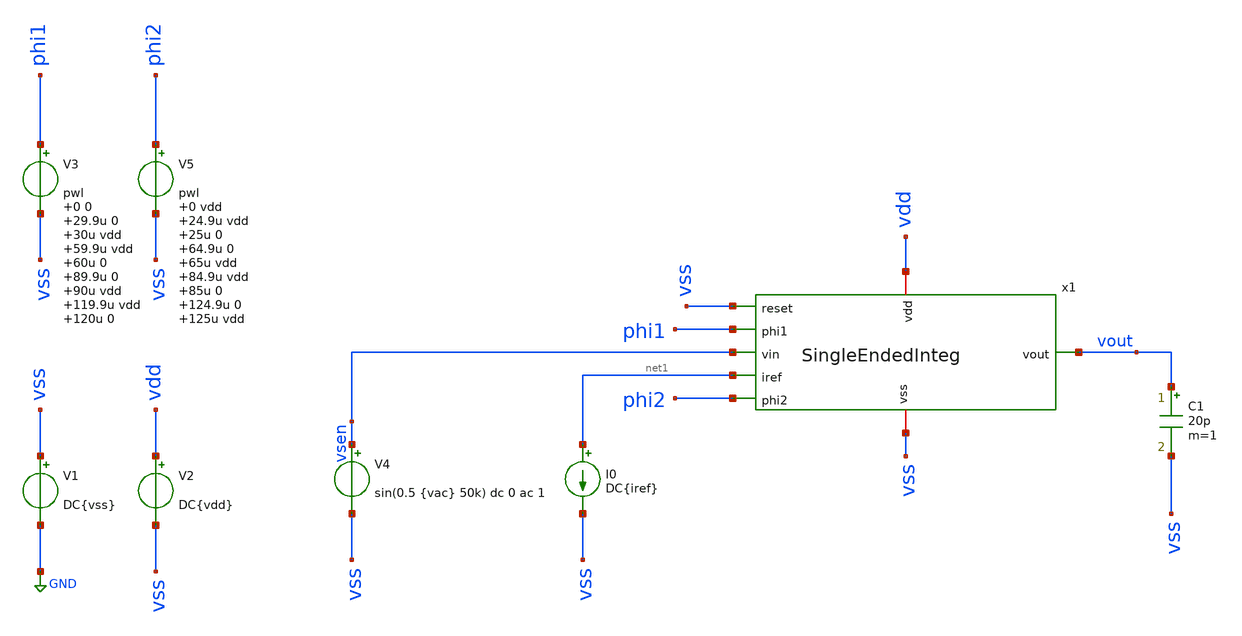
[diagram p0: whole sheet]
** sch_path: xschem/SinEndInteg_tb.sch
**.subckt SinEndInteg_tb
x1 vss phi1 vdd vsen vout net1 phi2 vss SingleEndedInteg
V1 vss GND DC{vss}
V2 vdd vss DC{vdd}
I0 net1 vss DC{iref}
C1 vout vss 20p m=1
V4 vsen vss sin(0.5 {vac} 50k) dc 0 ac 1
V3 phi1 vss pwl 0 0 29.9u 0 30u vdd 59.9u vdd 60u 0 89.9u 0 90u vdd 119.9u vdd 120u 0
V5 phi2 vss pwl 0 vdd 24.9u vdd 25u 0 64.9u 0 65u vdd 84.9u vdd 85u 0 124.9u 0 125u vdd
**** begin user architecture code




* Circuit Parameters
.param iref = 100u
.param vdd  = 1.8
.param vss  = 0.0
.param vcm  = 0.8
.param vac  = 0.5
.options TEMP = 65.0

* Include Models
.lib /foss/designs/PDK/sky130A/libs.tech/ngspice/sky130.lib.spice tt

* OP Parameters & Singals to save
.save all
*+ @M.X1.XM1.msky130_fd_pr__pfet_01v8[id] @M.X1.XM1.msky130_fd_pr__pfet_01v8[vth]
*+ @M.X1.XM1.msky130_fd_pr__pfet_01v8[vgs] @M.X1.XM1.msky130_fd_pr__pfet_01v8[vds] @M.X1.XM1.msky130_fd_pr__pfet_01v8[vdsat]
*+ @M.X1.XM1.msky130_fd_pr__pfet_01v8[gm] @M.X1.XM1.msky130_fd_pr__pfet_01v8[gds]
*+ @M.X1.XM2.msky130_fd_pr__pfet_01v8[id] @M.X1.XM2.msky130_fd_pr__pfet_01v8[vth]
*+ @M.X1.XM2.msky130_fd_pr__pfet_01v8[vgs] @M.X1.XM2.msky130_fd_pr__pfet_01v8[vds] @M.X1.XM2.msky130_fd_pr__pfet_01v8[vdsat]
*+ @M.X1.XM2.msky130_fd_pr__pfet_01v8[gm] @M.X1.XM2.msky130_fd_pr__pfet_01v8[gds]
*+ @M.X1.XM3.msky130_fd_pr__nfet_01v8[id] @M.X1.XM3.msky130_fd_pr__nfet_01v8[vth]
*+ @M.X1.XM3.msky130_fd_pr__nfet_01v8[vgs] @M.X1.XM3.msky130_fd_pr__nfet_01v8[vds] @M.X1.XM3.msky130_fd_pr__nfet_01v8[vdsat]
*+ @M.X1.XM3.msky130_fd_pr__nfet_01v8[gm] @M.X1.XM3.msky130_fd_pr__nfet_01v8[gds]
*+ @M.X1.XM4.msky130_fd_pr__nfet_01v8[id] @M.X1.XM4.msky130_fd_pr__nfet_01v8[vth]
*+ @M.X1.XM4.msky130_fd_pr__nfet_01v8[vgs] @M.X1.XM4.msky130_fd_pr__nfet_01v8[vds] @M.X1.XM4.msky130_fd_pr__nfet_01v8[vdsat]
*+ @M.X1.XM4.msky130_fd_pr__nfet_01v8[gm] @M.X1.XM4.msky130_fd_pr__nfet_01v8[gds]
*+ @M.X1.XM5.msky130_fd_pr__pfet_01v8[id] @M.X1.XM5.msky130_fd_pr__pfet_01v8[vth]
*+ @M.X1.XM5.msky130_fd_pr__pfet_01v8[vgs] @M.X1.XM5.msky130_fd_pr__pfet_01v8[vds] @M.X1.XM5.msky130_fd_pr__pfet_01v8[vdsat]
*+ @M.X1.XM5.msky130_fd_pr__pfet_01v8[gm] @M.X1.XM5.msky130_fd_pr__pfet_01v8[gds]
*+ @M.X1.XM6.msky130_fd_pr__nfet_01v8[id] @M.X1.XM6.msky130_fd_pr__nfet_01v8[vth]
*+ @M.X1.XM6.msky130_fd_pr__nfet_01v8[vgs] @M.X1.XM6.msky130_fd_pr__nfet_01v8[vds] @M.X1.XM6.msky130_fd_pr__nfet_01v8[vdsat]
*+ @M.X1.XM6.msky130_fd_pr__nfet_01v8[gm] @M.X1.XM6.msky130_fd_pr__nfet_01v8[gds]
*+ @M.X1.XM7.msky130_fd_pr__pfet_01v8[id] @M.X1.XM7.msky130_fd_pr__pfet_01v8[vth]
*+ @M.X1.XM7.msky130_fd_pr__pfet_01v8[vgs] @M.X1.XM7.msky130_fd_pr__pfet_01v8[vds] @M.X1.XM7.msky130_fd_pr__pfet_01v8[vdsat]
*+ @M.X1.XM7.msky130_fd_pr__pfet_01v8[gm] @M.X1.XM7.msky130_fd_pr__pfet_01v8[gds]
*+ @M.X1.XM8.msky130_fd_pr__pfet_01v8[id] @M.X1.XM8.msky130_fd_pr__pfet_01v8[vth]
*+ @M.X1.XM8.msky130_fd_pr__pfet_01v8[vgs] @M.X1.XM8.msky130_fd_pr__pfet_01v8[vds] @M.X1.XM8.msky130_fd_pr__pfet_01v8[vdsat]
*+ @M.X1.XM8.msky130_fd_pr__pfet_01v8[gm] @M.X1.XM8.msky130_fd_pr__pfet_01v8[gds]
*+ @M.X1.XM9.msky130_fd_pr__nfet_01v8[id] @M.X1.XM9.msky130_fd_pr__nfet_01v8[vth]
*+ @M.X1.XM9.msky130_fd_pr__nfet_01v8[vgs] @M.X1.XM9.msky130_fd_pr__nfet_01v8[vds] @M.X1.XM9.msky130_fd_pr__nfet_01v8[vdsat]
*+ @M.X1.XM9.msky130_fd_pr__nfet_01v8[gm] @M.X1.XM9.msky130_fd_pr__nfet_01v8[gds]

*Simulations
.control
  tran 0.01u 150u
  setplot tran1
  plot v(vsen) v(vout) v(phi1) v(phi2)
  write /foss/designs/SigmaDelta_ADC/xschem/sim_results/OpAmpinteg.raw

.endc

.end


**** end user architecture code
**.ends
.GLOBAL GND
.end
